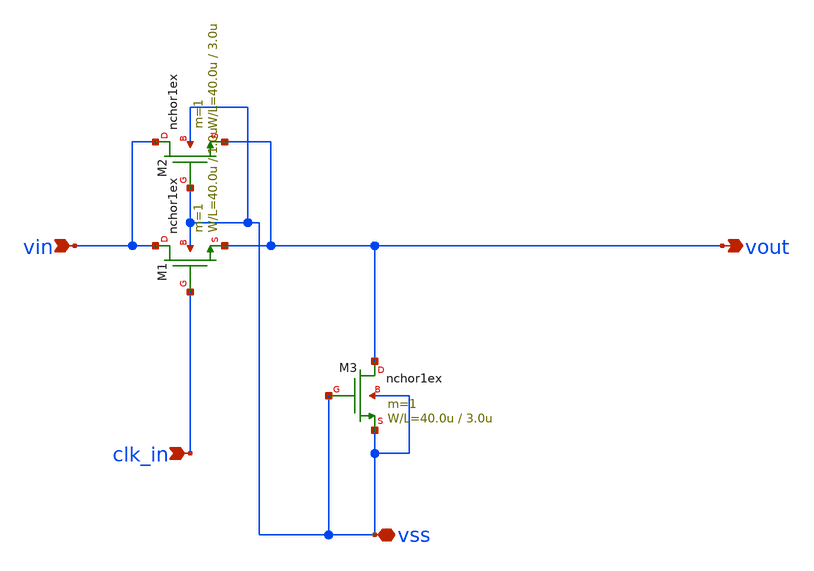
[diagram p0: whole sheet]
** sch_path: member_project/DCDC_DOWN/xschem/dcdc_base.sch
**.subckt dcdc_base clk_in vin vss vout
*.ipin clk_in
*.ipin vin
*.iopin vss
*.opin vout
M1 vin clk_in vout vss nchor1ex L=1.0u W=40.0u m=1
M2 vin vss vout vss nchor1ex L=3.0u W=40.0u m=1
M3 vout vss vss vss nchor1ex L=3.0u W=40.0u m=1
**.ends
.end
